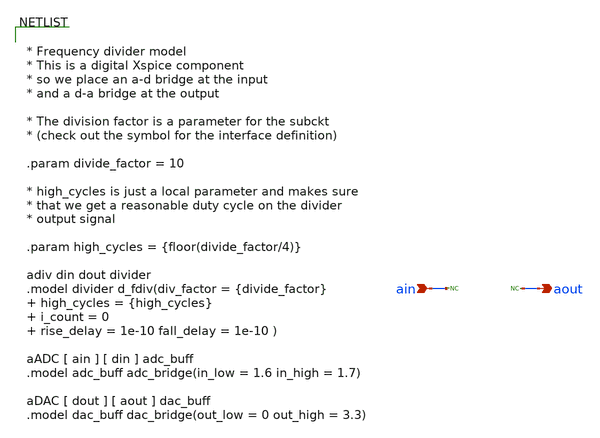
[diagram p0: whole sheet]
** sch_path: designs/libs/model_pll/freq_divider.sch
**.subckt freq_divider ain aout
*.ipin ain
*.opin aout
* noconn ain
* noconn aout
**** begin user architecture code


* Frequency divider model
* This is a digital Xspice component
* so we place an a-d bridge at the input
* and a d-a bridge at the output

* The division factor is a parameter for the subckt
* (check out the symbol for the interface definition)

.param divide_factor = 10

* high_cycles is just a local parameter and makes sure
* that we get a reasonable duty cycle on the divider
* output signal

.param high_cycles = {floor(divide_factor/4)}

adiv din dout divider
.model divider d_fdiv(div_factor = {divide_factor}  high_cycles = {high_cycles}   i_count = 0   rise_delay
+ = 1e-10 fall_delay = 1e-10 )

aADC [ ain ] [ din ] adc_buff
.model adc_buff adc_bridge(in_low = 1.6 in_high = 1.7)

aDAC [ dout ] [ aout ] dac_buff
.model dac_buff dac_bridge(out_low = 0 out_high = 3.3)



**** end user architecture code
**.ends
.end
